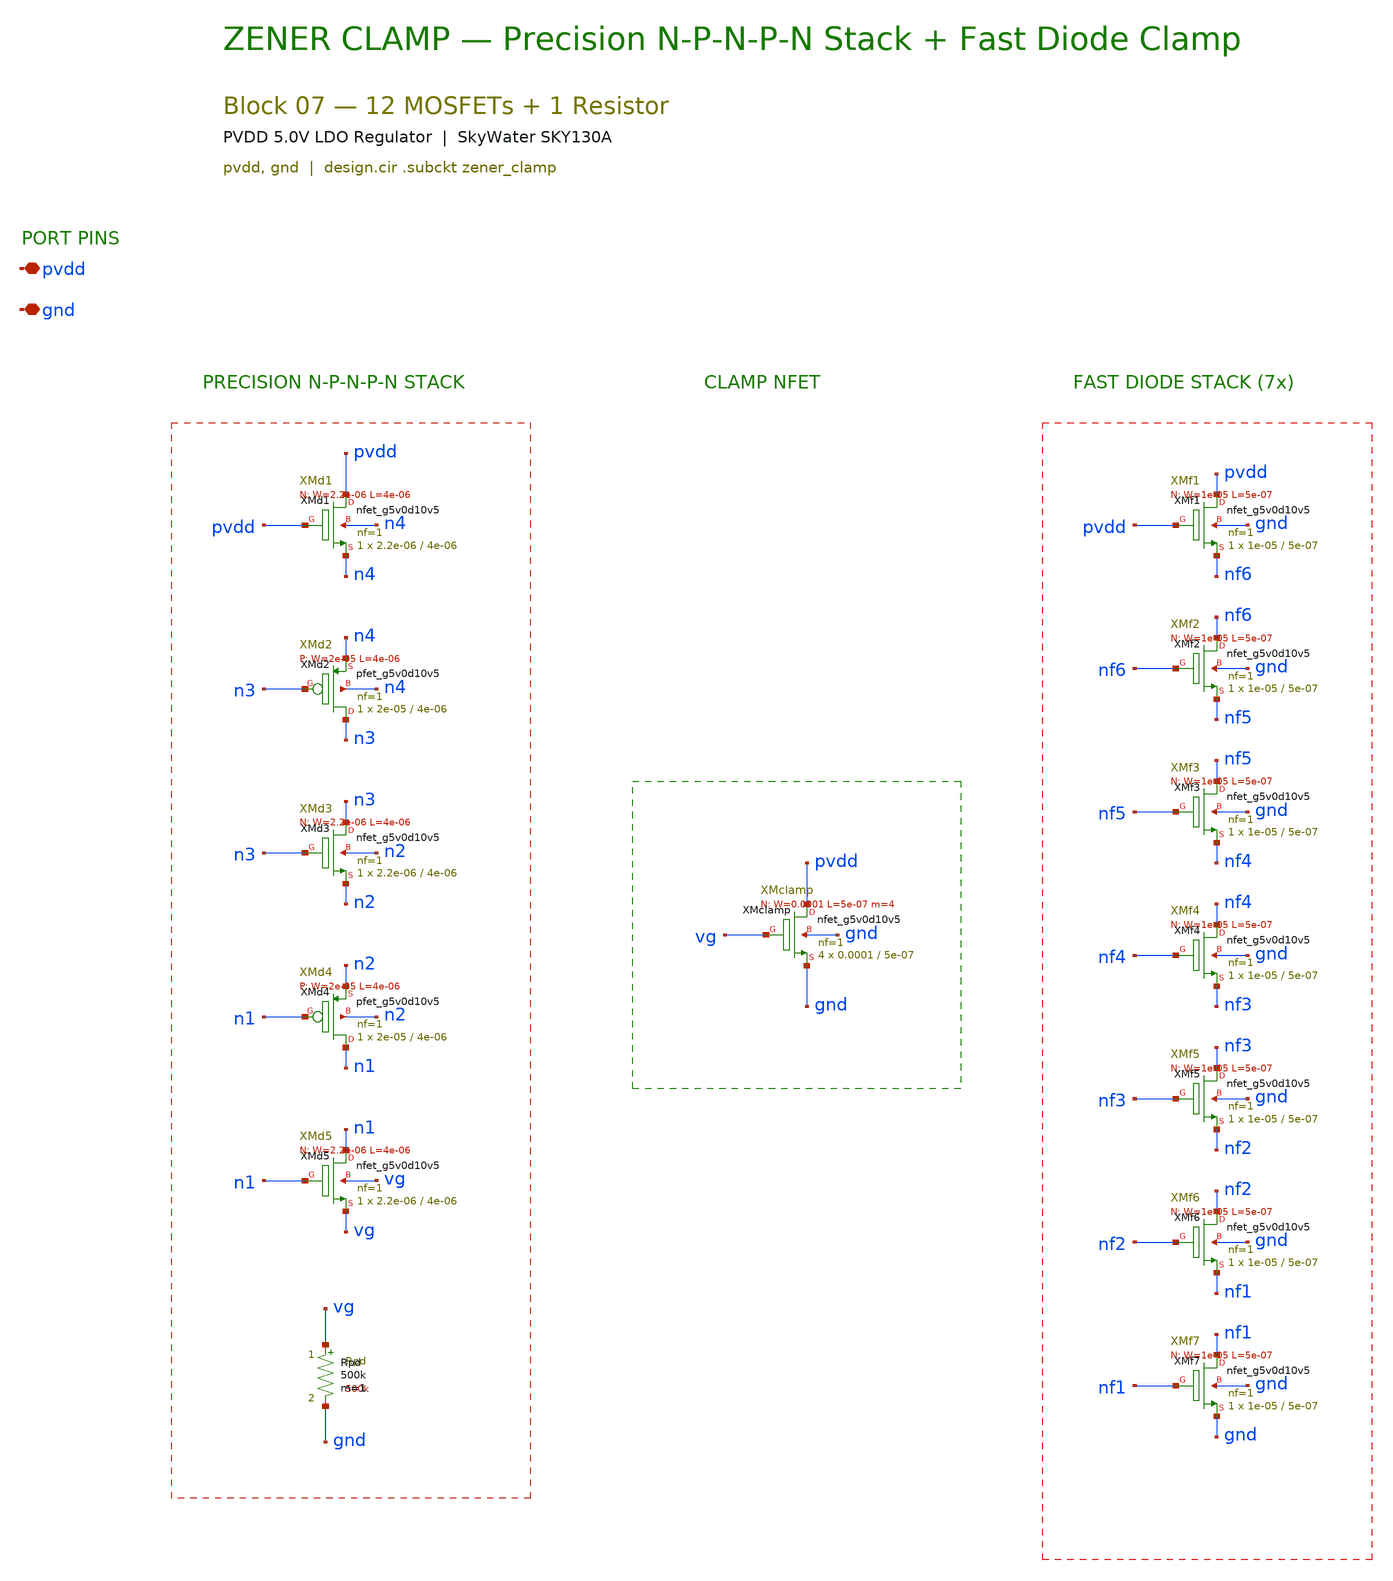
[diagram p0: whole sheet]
** sch_path: pvdd_regulator/10_top_integration/schematics/pvdd_07_zener_clamp.sch
**.subckt pvdd_07_zener_clamp pvdd gnd
*.iopin pvdd
*.iopin gnd
XXMd1 pvdd pvdd n4 n4 sky130_fd_pr__nfet_g5v0d10v5 L=4e-06 W=2.2e-06 nf=1 ad='int((1 + 1)/2) * 2.2e-06 / 1 * 0.29'
+ as='int((1 + 2)/2) * 2.2e-06 / 1 * 0.29' pd='2*int((1 + 1)/2) * (2.2e-06 / 1 + 0.29)' ps='2*int((1 + 2)/2) * (2.2e-06 / 1 + 0.29)'
+ nrd='0.29 / 2.2e-06 ' nrs='0.29 / 2.2e-06 ' sa=0 sb=0 sd=0 mult=1 m=1
XXMd2 n3 n3 n4 n4 sky130_fd_pr__pfet_g5v0d10v5 L=4e-06 W=2e-05 nf=1 ad='int((1 + 1)/2) * 2e-05 / 1 * 0.29'
+ as='int((1 + 2)/2) * 2e-05 / 1 * 0.29' pd='2*int((1 + 1)/2) * (2e-05 / 1 + 0.29)' ps='2*int((1 + 2)/2) * (2e-05 / 1 + 0.29)'
+ nrd='0.29 / 2e-05 ' nrs='0.29 / 2e-05 ' sa=0 sb=0 sd=0 mult=1 m=1
XXMd3 n3 n3 n2 n2 sky130_fd_pr__nfet_g5v0d10v5 L=4e-06 W=2.2e-06 nf=1 ad='int((1 + 1)/2) * 2.2e-06 / 1 * 0.29'
+ as='int((1 + 2)/2) * 2.2e-06 / 1 * 0.29' pd='2*int((1 + 1)/2) * (2.2e-06 / 1 + 0.29)' ps='2*int((1 + 2)/2) * (2.2e-06 / 1 + 0.29)'
+ nrd='0.29 / 2.2e-06 ' nrs='0.29 / 2.2e-06 ' sa=0 sb=0 sd=0 mult=1 m=1
XXMd4 n1 n1 n2 n2 sky130_fd_pr__pfet_g5v0d10v5 L=4e-06 W=2e-05 nf=1 ad='int((1 + 1)/2) * 2e-05 / 1 * 0.29'
+ as='int((1 + 2)/2) * 2e-05 / 1 * 0.29' pd='2*int((1 + 1)/2) * (2e-05 / 1 + 0.29)' ps='2*int((1 + 2)/2) * (2e-05 / 1 + 0.29)'
+ nrd='0.29 / 2e-05 ' nrs='0.29 / 2e-05 ' sa=0 sb=0 sd=0 mult=1 m=1
XXMd5 n1 n1 vg vg sky130_fd_pr__nfet_g5v0d10v5 L=4e-06 W=2.2e-06 nf=1 ad='int((1 + 1)/2) * 2.2e-06 / 1 * 0.29'
+ as='int((1 + 2)/2) * 2.2e-06 / 1 * 0.29' pd='2*int((1 + 1)/2) * (2.2e-06 / 1 + 0.29)' ps='2*int((1 + 2)/2) * (2.2e-06 / 1 + 0.29)'
+ nrd='0.29 / 2.2e-06 ' nrs='0.29 / 2.2e-06 ' sa=0 sb=0 sd=0 mult=1 m=1
Rpd vg gnd 500k m=1
XXMclamp pvdd vg gnd gnd sky130_fd_pr__nfet_g5v0d10v5 L=5e-07 W=0.0001 nf=1 ad='int((1 + 1)/2) * 0.0001 / 1 * 0.29'
+ as='int((1 + 2)/2) * 0.0001 / 1 * 0.29' pd='2*int((1 + 1)/2) * (0.0001 / 1 + 0.29)' ps='2*int((1 + 2)/2) * (0.0001 / 1 + 0.29)'
+ nrd='0.29 / 0.0001 ' nrs='0.29 / 0.0001 ' sa=0 sb=0 sd=0 mult=4 m=4
XXMf1 pvdd pvdd nf6 gnd sky130_fd_pr__nfet_g5v0d10v5 L=5e-07 W=1e-05 nf=1 ad='int((1 + 1)/2) * 1e-05 / 1 * 0.29'
+ as='int((1 + 2)/2) * 1e-05 / 1 * 0.29' pd='2*int((1 + 1)/2) * (1e-05 / 1 + 0.29)' ps='2*int((1 + 2)/2) * (1e-05 / 1 + 0.29)'
+ nrd='0.29 / 1e-05 ' nrs='0.29 / 1e-05 ' sa=0 sb=0 sd=0 mult=1 m=1
XXMf2 nf6 nf6 nf5 gnd sky130_fd_pr__nfet_g5v0d10v5 L=5e-07 W=1e-05 nf=1 ad='int((1 + 1)/2) * 1e-05 / 1 * 0.29'
+ as='int((1 + 2)/2) * 1e-05 / 1 * 0.29' pd='2*int((1 + 1)/2) * (1e-05 / 1 + 0.29)' ps='2*int((1 + 2)/2) * (1e-05 / 1 + 0.29)'
+ nrd='0.29 / 1e-05 ' nrs='0.29 / 1e-05 ' sa=0 sb=0 sd=0 mult=1 m=1
XXMf3 nf5 nf5 nf4 gnd sky130_fd_pr__nfet_g5v0d10v5 L=5e-07 W=1e-05 nf=1 ad='int((1 + 1)/2) * 1e-05 / 1 * 0.29'
+ as='int((1 + 2)/2) * 1e-05 / 1 * 0.29' pd='2*int((1 + 1)/2) * (1e-05 / 1 + 0.29)' ps='2*int((1 + 2)/2) * (1e-05 / 1 + 0.29)'
+ nrd='0.29 / 1e-05 ' nrs='0.29 / 1e-05 ' sa=0 sb=0 sd=0 mult=1 m=1
XXMf4 nf4 nf4 nf3 gnd sky130_fd_pr__nfet_g5v0d10v5 L=5e-07 W=1e-05 nf=1 ad='int((1 + 1)/2) * 1e-05 / 1 * 0.29'
+ as='int((1 + 2)/2) * 1e-05 / 1 * 0.29' pd='2*int((1 + 1)/2) * (1e-05 / 1 + 0.29)' ps='2*int((1 + 2)/2) * (1e-05 / 1 + 0.29)'
+ nrd='0.29 / 1e-05 ' nrs='0.29 / 1e-05 ' sa=0 sb=0 sd=0 mult=1 m=1
XXMf5 nf3 nf3 nf2 gnd sky130_fd_pr__nfet_g5v0d10v5 L=5e-07 W=1e-05 nf=1 ad='int((1 + 1)/2) * 1e-05 / 1 * 0.29'
+ as='int((1 + 2)/2) * 1e-05 / 1 * 0.29' pd='2*int((1 + 1)/2) * (1e-05 / 1 + 0.29)' ps='2*int((1 + 2)/2) * (1e-05 / 1 + 0.29)'
+ nrd='0.29 / 1e-05 ' nrs='0.29 / 1e-05 ' sa=0 sb=0 sd=0 mult=1 m=1
XXMf6 nf2 nf2 nf1 gnd sky130_fd_pr__nfet_g5v0d10v5 L=5e-07 W=1e-05 nf=1 ad='int((1 + 1)/2) * 1e-05 / 1 * 0.29'
+ as='int((1 + 2)/2) * 1e-05 / 1 * 0.29' pd='2*int((1 + 1)/2) * (1e-05 / 1 + 0.29)' ps='2*int((1 + 2)/2) * (1e-05 / 1 + 0.29)'
+ nrd='0.29 / 1e-05 ' nrs='0.29 / 1e-05 ' sa=0 sb=0 sd=0 mult=1 m=1
XXMf7 nf1 nf1 gnd gnd sky130_fd_pr__nfet_g5v0d10v5 L=5e-07 W=1e-05 nf=1 ad='int((1 + 1)/2) * 1e-05 / 1 * 0.29'
+ as='int((1 + 2)/2) * 1e-05 / 1 * 0.29' pd='2*int((1 + 1)/2) * (1e-05 / 1 + 0.29)' ps='2*int((1 + 2)/2) * (1e-05 / 1 + 0.29)'
+ nrd='0.29 / 1e-05 ' nrs='0.29 / 1e-05 ' sa=0 sb=0 sd=0 mult=1 m=1
**.ends
.end
